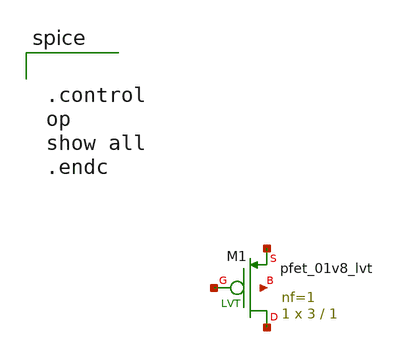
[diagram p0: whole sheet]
** sch_path: nmos.sch
**.subckt nmos
XM1 net1 net2 net3 net4 sky130_fd_pr__pfet_01v8_lvt L=1 W=3 nf=1 ad='int((nf+1)/2) * W/nf * 0.29' as='int((nf+2)/2) * W/nf * 0.29'
+ pd='2*int((nf+1)/2) * (W/nf + 0.29)' ps='2*int((nf+2)/2) * (W/nf + 0.29)' nrd='0.29 / W' nrs='0.29 / W'
+ sa=0 sb=0 sd=0 mult=1 m=1
**** begin user architecture code


.control
op
show all
.endc


*.lib ~/open_pdks/sky130/sky130A/libs.tech/ngspice/sky130.lib.spice tt
.param mc_mm_switch=0
.param mc_pr_switch=0

.include ~/open_pdks/sky130/sky130A/libs.tech/ngspice/corners/tt/nonfet.spice


*model
.include ~/open_pdks/sky130/sky130A/libs.tech/ngspice/all.spice

*mosfet
.include ~/open_pdks/sky130/sky130A/libs.ref/sky130_fd_pr/spice/sky130_fd_pr__pfet_01v8_lvt_tt.corner.spice
.inclued ~/open_pdks/sky130/sky130A/libs.ref/sky130_fd_pr/spice/sky130_fd_pr__nfet_01v8_lvt_tt.corner.spice

*mismatch parameters
.include ~/open_pdks/sky130/sky130A/libs.ref/sky130_fd_pr/spice/sky130_fd_pr__pfet_01v8_lvt__mismatch.corner.spice
.include ~/open_pdks/sky130/sky130A/libs.ref/sky130_fd_pr/spice/sky130_fd_pr__nfet_01v8_lvt__mismatch.corner.spice

**** end user architecture code
**.ends
.end
